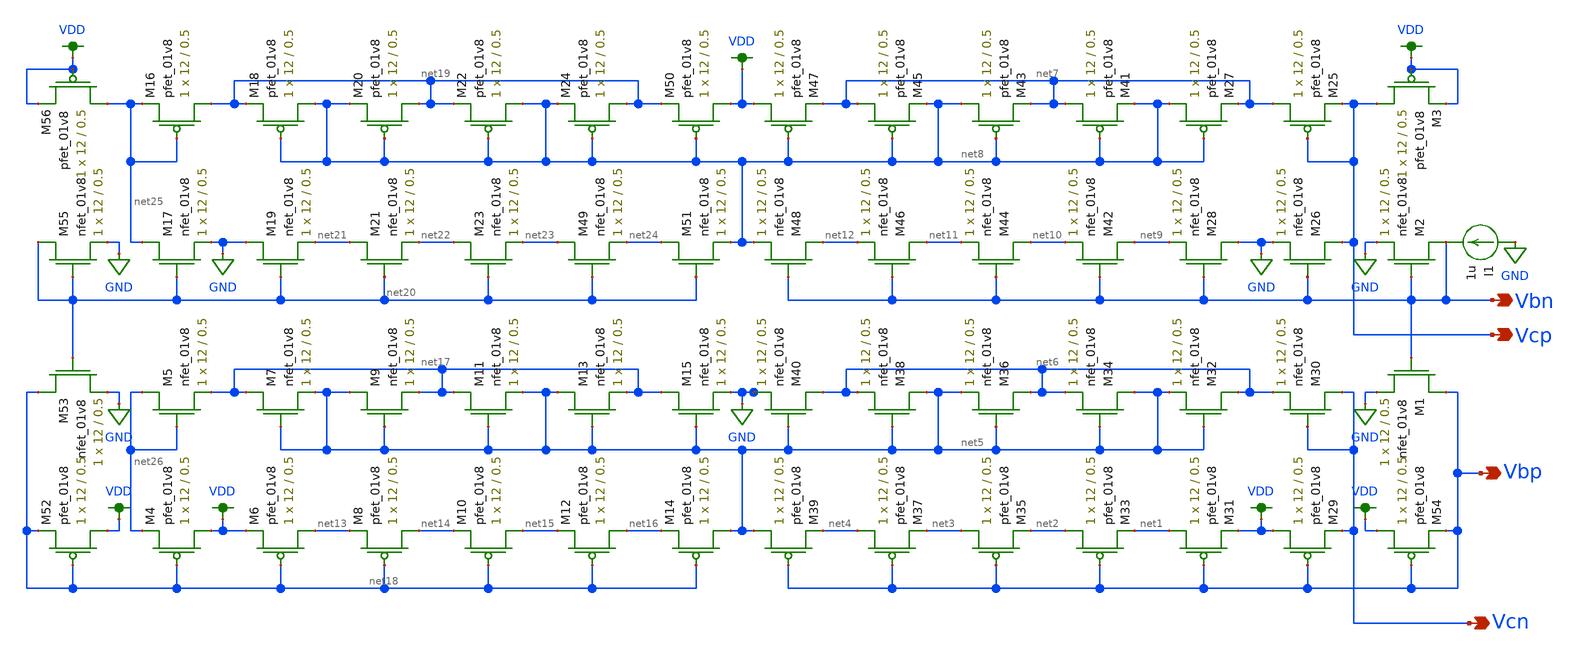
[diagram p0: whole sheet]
** sch_path: MP3/xschem/v_gen_lds.sch
**.subckt v_gen_lds Vcp Vcn Vbn Vbp
*.opin Vcp
*.opin Vcn
*.opin Vbn
*.opin Vbp
XM29 VDD Vbp Vcn VDD sky130_fd_pr__pfet_01v8 L=0.5 W=12 nf=1 ad='int((nf+1)/2) * W/nf * 0.29' as='int((nf+2)/2) * W/nf * 0.29'
+ pd='2*int((nf+1)/2) * (W/nf + 0.29)' ps='2*int((nf+2)/2) * (W/nf + 0.29)' nrd='0.29 / W' nrs='0.29 / W'
+ sa=0 sb=0 sd=0 mult=1 m=1
XM30 Vcn Vcn net6 GND sky130_fd_pr__nfet_01v8 L=0.5 W=12 nf=1 ad='int((nf+1)/2) * W/nf * 0.29' as='int((nf+2)/2) * W/nf * 0.29'
+ pd='2*int((nf+1)/2) * (W/nf + 0.29)' ps='2*int((nf+2)/2) * (W/nf + 0.29)' nrd='0.29 / W' nrs='0.29 / W'
+ sa=0 sb=0 sd=0 mult=1 m=1
XM31 net1 Vbp VDD VDD sky130_fd_pr__pfet_01v8 L=0.5 W=12 nf=1 ad='int((nf+1)/2) * W/nf * 0.29' as='int((nf+2)/2) * W/nf * 0.29'
+ pd='2*int((nf+1)/2) * (W/nf + 0.29)' ps='2*int((nf+2)/2) * (W/nf + 0.29)' nrd='0.29 / W' nrs='0.29 / W'
+ sa=0 sb=0 sd=0 mult=1 m=1
XM32 net6 net5 net5 GND sky130_fd_pr__nfet_01v8 L=0.5 W=12 nf=1 ad='int((nf+1)/2) * W/nf * 0.29' as='int((nf+2)/2) * W/nf * 0.29'
+ pd='2*int((nf+1)/2) * (W/nf + 0.29)' ps='2*int((nf+2)/2) * (W/nf + 0.29)' nrd='0.29 / W' nrs='0.29 / W'
+ sa=0 sb=0 sd=0 mult=1 m=1
XM33 net2 Vbp net1 VDD sky130_fd_pr__pfet_01v8 L=0.5 W=12 nf=1 ad='int((nf+1)/2) * W/nf * 0.29' as='int((nf+2)/2) * W/nf * 0.29'
+ pd='2*int((nf+1)/2) * (W/nf + 0.29)' ps='2*int((nf+2)/2) * (W/nf + 0.29)' nrd='0.29 / W' nrs='0.29 / W'
+ sa=0 sb=0 sd=0 mult=1 m=1
XM34 net5 net5 net6 GND sky130_fd_pr__nfet_01v8 L=0.5 W=12 nf=1 ad='int((nf+1)/2) * W/nf * 0.29' as='int((nf+2)/2) * W/nf * 0.29'
+ pd='2*int((nf+1)/2) * (W/nf + 0.29)' ps='2*int((nf+2)/2) * (W/nf + 0.29)' nrd='0.29 / W' nrs='0.29 / W'
+ sa=0 sb=0 sd=0 mult=1 m=1
XM35 net3 Vbp net2 VDD sky130_fd_pr__pfet_01v8 L=0.5 W=12 nf=1 ad='int((nf+1)/2) * W/nf * 0.29' as='int((nf+2)/2) * W/nf * 0.29'
+ pd='2*int((nf+1)/2) * (W/nf + 0.29)' ps='2*int((nf+2)/2) * (W/nf + 0.29)' nrd='0.29 / W' nrs='0.29 / W'
+ sa=0 sb=0 sd=0 mult=1 m=1
XM36 net6 net5 net5 GND sky130_fd_pr__nfet_01v8 L=0.5 W=12 nf=1 ad='int((nf+1)/2) * W/nf * 0.29' as='int((nf+2)/2) * W/nf * 0.29'
+ pd='2*int((nf+1)/2) * (W/nf + 0.29)' ps='2*int((nf+2)/2) * (W/nf + 0.29)' nrd='0.29 / W' nrs='0.29 / W'
+ sa=0 sb=0 sd=0 mult=1 m=1
XM37 net4 Vbp net3 VDD sky130_fd_pr__pfet_01v8 L=0.5 W=12 nf=1 ad='int((nf+1)/2) * W/nf * 0.29' as='int((nf+2)/2) * W/nf * 0.29'
+ pd='2*int((nf+1)/2) * (W/nf + 0.29)' ps='2*int((nf+2)/2) * (W/nf + 0.29)' nrd='0.29 / W' nrs='0.29 / W'
+ sa=0 sb=0 sd=0 mult=1 m=1
XM38 net5 net5 net6 GND sky130_fd_pr__nfet_01v8 L=0.5 W=12 nf=1 ad='int((nf+1)/2) * W/nf * 0.29' as='int((nf+2)/2) * W/nf * 0.29'
+ pd='2*int((nf+1)/2) * (W/nf + 0.29)' ps='2*int((nf+2)/2) * (W/nf + 0.29)' nrd='0.29 / W' nrs='0.29 / W'
+ sa=0 sb=0 sd=0 mult=1 m=1
XM39 net5 Vbp net4 VDD sky130_fd_pr__pfet_01v8 L=0.5 W=12 nf=1 ad='int((nf+1)/2) * W/nf * 0.29' as='int((nf+2)/2) * W/nf * 0.29'
+ pd='2*int((nf+1)/2) * (W/nf + 0.29)' ps='2*int((nf+2)/2) * (W/nf + 0.29)' nrd='0.29 / W' nrs='0.29 / W'
+ sa=0 sb=0 sd=0 mult=1 m=1
XM40 net6 net5 GND GND sky130_fd_pr__nfet_01v8 L=0.5 W=12 nf=1 ad='int((nf+1)/2) * W/nf * 0.29' as='int((nf+2)/2) * W/nf * 0.29'
+ pd='2*int((nf+1)/2) * (W/nf + 0.29)' ps='2*int((nf+2)/2) * (W/nf + 0.29)' nrd='0.29 / W' nrs='0.29 / W'
+ sa=0 sb=0 sd=0 mult=1 m=1
XM25 net7 Vcp Vcp VDD sky130_fd_pr__pfet_01v8 L=0.5 W=12 nf=1 ad='int((nf+1)/2) * W/nf * 0.29' as='int((nf+2)/2) * W/nf * 0.29'
+ pd='2*int((nf+1)/2) * (W/nf + 0.29)' ps='2*int((nf+2)/2) * (W/nf + 0.29)' nrd='0.29 / W' nrs='0.29 / W'
+ sa=0 sb=0 sd=0 mult=1 m=1
XM26 Vcp Vbn GND GND sky130_fd_pr__nfet_01v8 L=0.5 W=12 nf=1 ad='int((nf+1)/2) * W/nf * 0.29' as='int((nf+2)/2) * W/nf * 0.29'
+ pd='2*int((nf+1)/2) * (W/nf + 0.29)' ps='2*int((nf+2)/2) * (W/nf + 0.29)' nrd='0.29 / W' nrs='0.29 / W'
+ sa=0 sb=0 sd=0 mult=1 m=1
XM27 net8 net8 net7 VDD sky130_fd_pr__pfet_01v8 L=0.5 W=12 nf=1 ad='int((nf+1)/2) * W/nf * 0.29' as='int((nf+2)/2) * W/nf * 0.29'
+ pd='2*int((nf+1)/2) * (W/nf + 0.29)' ps='2*int((nf+2)/2) * (W/nf + 0.29)' nrd='0.29 / W' nrs='0.29 / W'
+ sa=0 sb=0 sd=0 mult=1 m=1
XM28 GND Vbn net9 GND sky130_fd_pr__nfet_01v8 L=0.5 W=12 nf=1 ad='int((nf+1)/2) * W/nf * 0.29' as='int((nf+2)/2) * W/nf * 0.29'
+ pd='2*int((nf+1)/2) * (W/nf + 0.29)' ps='2*int((nf+2)/2) * (W/nf + 0.29)' nrd='0.29 / W' nrs='0.29 / W'
+ sa=0 sb=0 sd=0 mult=1 m=1
XM41 net7 net8 net8 VDD sky130_fd_pr__pfet_01v8 L=0.5 W=12 nf=1 ad='int((nf+1)/2) * W/nf * 0.29' as='int((nf+2)/2) * W/nf * 0.29'
+ pd='2*int((nf+1)/2) * (W/nf + 0.29)' ps='2*int((nf+2)/2) * (W/nf + 0.29)' nrd='0.29 / W' nrs='0.29 / W'
+ sa=0 sb=0 sd=0 mult=1 m=1
XM42 net9 Vbn net10 GND sky130_fd_pr__nfet_01v8 L=0.5 W=12 nf=1 ad='int((nf+1)/2) * W/nf * 0.29' as='int((nf+2)/2) * W/nf * 0.29'
+ pd='2*int((nf+1)/2) * (W/nf + 0.29)' ps='2*int((nf+2)/2) * (W/nf + 0.29)' nrd='0.29 / W' nrs='0.29 / W'
+ sa=0 sb=0 sd=0 mult=1 m=1
XM43 net8 net8 net7 VDD sky130_fd_pr__pfet_01v8 L=0.5 W=12 nf=1 ad='int((nf+1)/2) * W/nf * 0.29' as='int((nf+2)/2) * W/nf * 0.29'
+ pd='2*int((nf+1)/2) * (W/nf + 0.29)' ps='2*int((nf+2)/2) * (W/nf + 0.29)' nrd='0.29 / W' nrs='0.29 / W'
+ sa=0 sb=0 sd=0 mult=1 m=1
XM44 net10 Vbn net11 GND sky130_fd_pr__nfet_01v8 L=0.5 W=12 nf=1 ad='int((nf+1)/2) * W/nf * 0.29' as='int((nf+2)/2) * W/nf * 0.29'
+ pd='2*int((nf+1)/2) * (W/nf + 0.29)' ps='2*int((nf+2)/2) * (W/nf + 0.29)' nrd='0.29 / W' nrs='0.29 / W'
+ sa=0 sb=0 sd=0 mult=1 m=1
XM45 net7 net8 net8 VDD sky130_fd_pr__pfet_01v8 L=0.5 W=12 nf=1 ad='int((nf+1)/2) * W/nf * 0.29' as='int((nf+2)/2) * W/nf * 0.29'
+ pd='2*int((nf+1)/2) * (W/nf + 0.29)' ps='2*int((nf+2)/2) * (W/nf + 0.29)' nrd='0.29 / W' nrs='0.29 / W'
+ sa=0 sb=0 sd=0 mult=1 m=1
XM46 net11 Vbn net12 GND sky130_fd_pr__nfet_01v8 L=0.5 W=12 nf=1 ad='int((nf+1)/2) * W/nf * 0.29' as='int((nf+2)/2) * W/nf * 0.29'
+ pd='2*int((nf+1)/2) * (W/nf + 0.29)' ps='2*int((nf+2)/2) * (W/nf + 0.29)' nrd='0.29 / W' nrs='0.29 / W'
+ sa=0 sb=0 sd=0 mult=1 m=1
XM47 VDD net8 net7 VDD sky130_fd_pr__pfet_01v8 L=0.5 W=12 nf=1 ad='int((nf+1)/2) * W/nf * 0.29' as='int((nf+2)/2) * W/nf * 0.29'
+ pd='2*int((nf+1)/2) * (W/nf + 0.29)' ps='2*int((nf+2)/2) * (W/nf + 0.29)' nrd='0.29 / W' nrs='0.29 / W'
+ sa=0 sb=0 sd=0 mult=1 m=1
XM48 net12 Vbn net8 GND sky130_fd_pr__nfet_01v8 L=0.5 W=12 nf=1 ad='int((nf+1)/2) * W/nf * 0.29' as='int((nf+2)/2) * W/nf * 0.29'
+ pd='2*int((nf+1)/2) * (W/nf + 0.29)' ps='2*int((nf+2)/2) * (W/nf + 0.29)' nrd='0.29 / W' nrs='0.29 / W'
+ sa=0 sb=0 sd=0 mult=1 m=1
XM54 VDD Vbp Vbp VDD sky130_fd_pr__pfet_01v8 L=0.5 W=12 nf=1 ad='int((nf+1)/2) * W/nf * 0.29' as='int((nf+2)/2) * W/nf * 0.29'
+ pd='2*int((nf+1)/2) * (W/nf + 0.29)' ps='2*int((nf+2)/2) * (W/nf + 0.29)' nrd='0.29 / W' nrs='0.29 / W'
+ sa=0 sb=0 sd=0 mult=1 m=1
XM1 Vbp Vbn GND GND sky130_fd_pr__nfet_01v8 L=0.5 W=12 nf=1 ad='int((nf+1)/2) * W/nf * 0.29' as='int((nf+2)/2) * W/nf * 0.29'
+ pd='2*int((nf+1)/2) * (W/nf + 0.29)' ps='2*int((nf+2)/2) * (W/nf + 0.29)' nrd='0.29 / W' nrs='0.29 / W'
+ sa=0 sb=0 sd=0 mult=1 m=1
XM2 Vbn Vbn GND GND sky130_fd_pr__nfet_01v8 L=0.5 W=12 nf=1 ad='int((nf+1)/2) * W/nf * 0.29' as='int((nf+2)/2) * W/nf * 0.29'
+ pd='2*int((nf+1)/2) * (W/nf + 0.29)' ps='2*int((nf+2)/2) * (W/nf + 0.29)' nrd='0.29 / W' nrs='0.29 / W'
+ sa=0 sb=0 sd=0 mult=1 m=1
XM3 Vcp VDD VDD VDD sky130_fd_pr__pfet_01v8 L=0.5 W=12 nf=1 ad='int((nf+1)/2) * W/nf * 0.29' as='int((nf+2)/2) * W/nf * 0.29'
+ pd='2*int((nf+1)/2) * (W/nf + 0.29)' ps='2*int((nf+2)/2) * (W/nf + 0.29)' nrd='0.29 / W' nrs='0.29 / W'
+ sa=0 sb=0 sd=0 mult=1 m=1
XM4 VDD net18 net26 VDD sky130_fd_pr__pfet_01v8 L=0.5 W=12 nf=1 ad='int((nf+1)/2) * W/nf * 0.29' as='int((nf+2)/2) * W/nf * 0.29'
+ pd='2*int((nf+1)/2) * (W/nf + 0.29)' ps='2*int((nf+2)/2) * (W/nf + 0.29)' nrd='0.29 / W' nrs='0.29 / W'
+ sa=0 sb=0 sd=0 mult=1 m=1
XM5 net26 net26 net17 GND sky130_fd_pr__nfet_01v8 L=0.5 W=12 nf=1 ad='int((nf+1)/2) * W/nf * 0.29' as='int((nf+2)/2) * W/nf * 0.29'
+ pd='2*int((nf+1)/2) * (W/nf + 0.29)' ps='2*int((nf+2)/2) * (W/nf + 0.29)' nrd='0.29 / W' nrs='0.29 / W'
+ sa=0 sb=0 sd=0 mult=1 m=1
XM6 net13 net18 VDD VDD sky130_fd_pr__pfet_01v8 L=0.5 W=12 nf=1 ad='int((nf+1)/2) * W/nf * 0.29' as='int((nf+2)/2) * W/nf * 0.29'
+ pd='2*int((nf+1)/2) * (W/nf + 0.29)' ps='2*int((nf+2)/2) * (W/nf + 0.29)' nrd='0.29 / W' nrs='0.29 / W'
+ sa=0 sb=0 sd=0 mult=1 m=1
XM7 net17 net5 net5 GND sky130_fd_pr__nfet_01v8 L=0.5 W=12 nf=1 ad='int((nf+1)/2) * W/nf * 0.29' as='int((nf+2)/2) * W/nf * 0.29'
+ pd='2*int((nf+1)/2) * (W/nf + 0.29)' ps='2*int((nf+2)/2) * (W/nf + 0.29)' nrd='0.29 / W' nrs='0.29 / W'
+ sa=0 sb=0 sd=0 mult=1 m=1
XM8 net14 net18 net13 VDD sky130_fd_pr__pfet_01v8 L=0.5 W=12 nf=1 ad='int((nf+1)/2) * W/nf * 0.29' as='int((nf+2)/2) * W/nf * 0.29'
+ pd='2*int((nf+1)/2) * (W/nf + 0.29)' ps='2*int((nf+2)/2) * (W/nf + 0.29)' nrd='0.29 / W' nrs='0.29 / W'
+ sa=0 sb=0 sd=0 mult=1 m=1
XM9 net5 net5 net17 GND sky130_fd_pr__nfet_01v8 L=0.5 W=12 nf=1 ad='int((nf+1)/2) * W/nf * 0.29' as='int((nf+2)/2) * W/nf * 0.29'
+ pd='2*int((nf+1)/2) * (W/nf + 0.29)' ps='2*int((nf+2)/2) * (W/nf + 0.29)' nrd='0.29 / W' nrs='0.29 / W'
+ sa=0 sb=0 sd=0 mult=1 m=1
XM10 net15 net18 net14 VDD sky130_fd_pr__pfet_01v8 L=0.5 W=12 nf=1 ad='int((nf+1)/2) * W/nf * 0.29' as='int((nf+2)/2) * W/nf * 0.29'
+ pd='2*int((nf+1)/2) * (W/nf + 0.29)' ps='2*int((nf+2)/2) * (W/nf + 0.29)' nrd='0.29 / W' nrs='0.29 / W'
+ sa=0 sb=0 sd=0 mult=1 m=1
XM11 net17 net5 net5 GND sky130_fd_pr__nfet_01v8 L=0.5 W=12 nf=1 ad='int((nf+1)/2) * W/nf * 0.29' as='int((nf+2)/2) * W/nf * 0.29'
+ pd='2*int((nf+1)/2) * (W/nf + 0.29)' ps='2*int((nf+2)/2) * (W/nf + 0.29)' nrd='0.29 / W' nrs='0.29 / W'
+ sa=0 sb=0 sd=0 mult=1 m=1
XM12 net16 net18 net15 VDD sky130_fd_pr__pfet_01v8 L=0.5 W=12 nf=1 ad='int((nf+1)/2) * W/nf * 0.29' as='int((nf+2)/2) * W/nf * 0.29'
+ pd='2*int((nf+1)/2) * (W/nf + 0.29)' ps='2*int((nf+2)/2) * (W/nf + 0.29)' nrd='0.29 / W' nrs='0.29 / W'
+ sa=0 sb=0 sd=0 mult=1 m=1
XM13 net5 net5 net17 GND sky130_fd_pr__nfet_01v8 L=0.5 W=12 nf=1 ad='int((nf+1)/2) * W/nf * 0.29' as='int((nf+2)/2) * W/nf * 0.29'
+ pd='2*int((nf+1)/2) * (W/nf + 0.29)' ps='2*int((nf+2)/2) * (W/nf + 0.29)' nrd='0.29 / W' nrs='0.29 / W'
+ sa=0 sb=0 sd=0 mult=1 m=1
XM14 net5 net18 net16 VDD sky130_fd_pr__pfet_01v8 L=0.5 W=12 nf=1 ad='int((nf+1)/2) * W/nf * 0.29' as='int((nf+2)/2) * W/nf * 0.29'
+ pd='2*int((nf+1)/2) * (W/nf + 0.29)' ps='2*int((nf+2)/2) * (W/nf + 0.29)' nrd='0.29 / W' nrs='0.29 / W'
+ sa=0 sb=0 sd=0 mult=1 m=1
XM15 net17 net5 GND GND sky130_fd_pr__nfet_01v8 L=0.5 W=12 nf=1 ad='int((nf+1)/2) * W/nf * 0.29' as='int((nf+2)/2) * W/nf * 0.29'
+ pd='2*int((nf+1)/2) * (W/nf + 0.29)' ps='2*int((nf+2)/2) * (W/nf + 0.29)' nrd='0.29 / W' nrs='0.29 / W'
+ sa=0 sb=0 sd=0 mult=1 m=1
XM16 net19 net25 net25 VDD sky130_fd_pr__pfet_01v8 L=0.5 W=12 nf=1 ad='int((nf+1)/2) * W/nf * 0.29' as='int((nf+2)/2) * W/nf * 0.29'
+ pd='2*int((nf+1)/2) * (W/nf + 0.29)' ps='2*int((nf+2)/2) * (W/nf + 0.29)' nrd='0.29 / W' nrs='0.29 / W'
+ sa=0 sb=0 sd=0 mult=1 m=1
XM17 net25 net20 GND GND sky130_fd_pr__nfet_01v8 L=0.5 W=12 nf=1 ad='int((nf+1)/2) * W/nf * 0.29' as='int((nf+2)/2) * W/nf * 0.29'
+ pd='2*int((nf+1)/2) * (W/nf + 0.29)' ps='2*int((nf+2)/2) * (W/nf + 0.29)' nrd='0.29 / W' nrs='0.29 / W'
+ sa=0 sb=0 sd=0 mult=1 m=1
XM18 net8 net8 net19 VDD sky130_fd_pr__pfet_01v8 L=0.5 W=12 nf=1 ad='int((nf+1)/2) * W/nf * 0.29' as='int((nf+2)/2) * W/nf * 0.29'
+ pd='2*int((nf+1)/2) * (W/nf + 0.29)' ps='2*int((nf+2)/2) * (W/nf + 0.29)' nrd='0.29 / W' nrs='0.29 / W'
+ sa=0 sb=0 sd=0 mult=1 m=1
XM19 GND net20 net21 GND sky130_fd_pr__nfet_01v8 L=0.5 W=12 nf=1 ad='int((nf+1)/2) * W/nf * 0.29' as='int((nf+2)/2) * W/nf * 0.29'
+ pd='2*int((nf+1)/2) * (W/nf + 0.29)' ps='2*int((nf+2)/2) * (W/nf + 0.29)' nrd='0.29 / W' nrs='0.29 / W'
+ sa=0 sb=0 sd=0 mult=1 m=1
XM20 net19 net8 net8 VDD sky130_fd_pr__pfet_01v8 L=0.5 W=12 nf=1 ad='int((nf+1)/2) * W/nf * 0.29' as='int((nf+2)/2) * W/nf * 0.29'
+ pd='2*int((nf+1)/2) * (W/nf + 0.29)' ps='2*int((nf+2)/2) * (W/nf + 0.29)' nrd='0.29 / W' nrs='0.29 / W'
+ sa=0 sb=0 sd=0 mult=1 m=1
XM21 net21 net20 net22 GND sky130_fd_pr__nfet_01v8 L=0.5 W=12 nf=1 ad='int((nf+1)/2) * W/nf * 0.29' as='int((nf+2)/2) * W/nf * 0.29'
+ pd='2*int((nf+1)/2) * (W/nf + 0.29)' ps='2*int((nf+2)/2) * (W/nf + 0.29)' nrd='0.29 / W' nrs='0.29 / W'
+ sa=0 sb=0 sd=0 mult=1 m=1
XM22 net8 net8 net19 VDD sky130_fd_pr__pfet_01v8 L=0.5 W=12 nf=1 ad='int((nf+1)/2) * W/nf * 0.29' as='int((nf+2)/2) * W/nf * 0.29'
+ pd='2*int((nf+1)/2) * (W/nf + 0.29)' ps='2*int((nf+2)/2) * (W/nf + 0.29)' nrd='0.29 / W' nrs='0.29 / W'
+ sa=0 sb=0 sd=0 mult=1 m=1
XM23 net22 net20 net23 GND sky130_fd_pr__nfet_01v8 L=0.5 W=12 nf=1 ad='int((nf+1)/2) * W/nf * 0.29' as='int((nf+2)/2) * W/nf * 0.29'
+ pd='2*int((nf+1)/2) * (W/nf + 0.29)' ps='2*int((nf+2)/2) * (W/nf + 0.29)' nrd='0.29 / W' nrs='0.29 / W'
+ sa=0 sb=0 sd=0 mult=1 m=1
XM24 net19 net8 net8 VDD sky130_fd_pr__pfet_01v8 L=0.5 W=12 nf=1 ad='int((nf+1)/2) * W/nf * 0.29' as='int((nf+2)/2) * W/nf * 0.29'
+ pd='2*int((nf+1)/2) * (W/nf + 0.29)' ps='2*int((nf+2)/2) * (W/nf + 0.29)' nrd='0.29 / W' nrs='0.29 / W'
+ sa=0 sb=0 sd=0 mult=1 m=1
XM49 net23 net20 net24 GND sky130_fd_pr__nfet_01v8 L=0.5 W=12 nf=1 ad='int((nf+1)/2) * W/nf * 0.29' as='int((nf+2)/2) * W/nf * 0.29'
+ pd='2*int((nf+1)/2) * (W/nf + 0.29)' ps='2*int((nf+2)/2) * (W/nf + 0.29)' nrd='0.29 / W' nrs='0.29 / W'
+ sa=0 sb=0 sd=0 mult=1 m=1
XM50 VDD net8 net19 VDD sky130_fd_pr__pfet_01v8 L=0.5 W=12 nf=1 ad='int((nf+1)/2) * W/nf * 0.29' as='int((nf+2)/2) * W/nf * 0.29'
+ pd='2*int((nf+1)/2) * (W/nf + 0.29)' ps='2*int((nf+2)/2) * (W/nf + 0.29)' nrd='0.29 / W' nrs='0.29 / W'
+ sa=0 sb=0 sd=0 mult=1 m=1
XM51 net24 net20 net8 GND sky130_fd_pr__nfet_01v8 L=0.5 W=12 nf=1 ad='int((nf+1)/2) * W/nf * 0.29' as='int((nf+2)/2) * W/nf * 0.29'
+ pd='2*int((nf+1)/2) * (W/nf + 0.29)' ps='2*int((nf+2)/2) * (W/nf + 0.29)' nrd='0.29 / W' nrs='0.29 / W'
+ sa=0 sb=0 sd=0 mult=1 m=1
XM52 VDD net18 net18 VDD sky130_fd_pr__pfet_01v8 L=0.5 W=12 nf=1 ad='int((nf+1)/2) * W/nf * 0.29' as='int((nf+2)/2) * W/nf * 0.29'
+ pd='2*int((nf+1)/2) * (W/nf + 0.29)' ps='2*int((nf+2)/2) * (W/nf + 0.29)' nrd='0.29 / W' nrs='0.29 / W'
+ sa=0 sb=0 sd=0 mult=1 m=1
XM53 net18 net20 GND GND sky130_fd_pr__nfet_01v8 L=0.5 W=12 nf=1 ad='int((nf+1)/2) * W/nf * 0.29' as='int((nf+2)/2) * W/nf * 0.29'
+ pd='2*int((nf+1)/2) * (W/nf + 0.29)' ps='2*int((nf+2)/2) * (W/nf + 0.29)' nrd='0.29 / W' nrs='0.29 / W'
+ sa=0 sb=0 sd=0 mult=1 m=1
XM55 net20 net20 GND GND sky130_fd_pr__nfet_01v8 L=0.5 W=12 nf=1 ad='int((nf+1)/2) * W/nf * 0.29' as='int((nf+2)/2) * W/nf * 0.29'
+ pd='2*int((nf+1)/2) * (W/nf + 0.29)' ps='2*int((nf+2)/2) * (W/nf + 0.29)' nrd='0.29 / W' nrs='0.29 / W'
+ sa=0 sb=0 sd=0 mult=1 m=1
XM56 net25 VDD VDD VDD sky130_fd_pr__pfet_01v8 L=0.5 W=12 nf=1 ad='int((nf+1)/2) * W/nf * 0.29' as='int((nf+2)/2) * W/nf * 0.29'
+ pd='2*int((nf+1)/2) * (W/nf + 0.29)' ps='2*int((nf+2)/2) * (W/nf + 0.29)' nrd='0.29 / W' nrs='0.29 / W'
+ sa=0 sb=0 sd=0 mult=1 m=1
I1 GND Vbn 1u
**.ends
.GLOBAL VDD
.GLOBAL GND
.end
